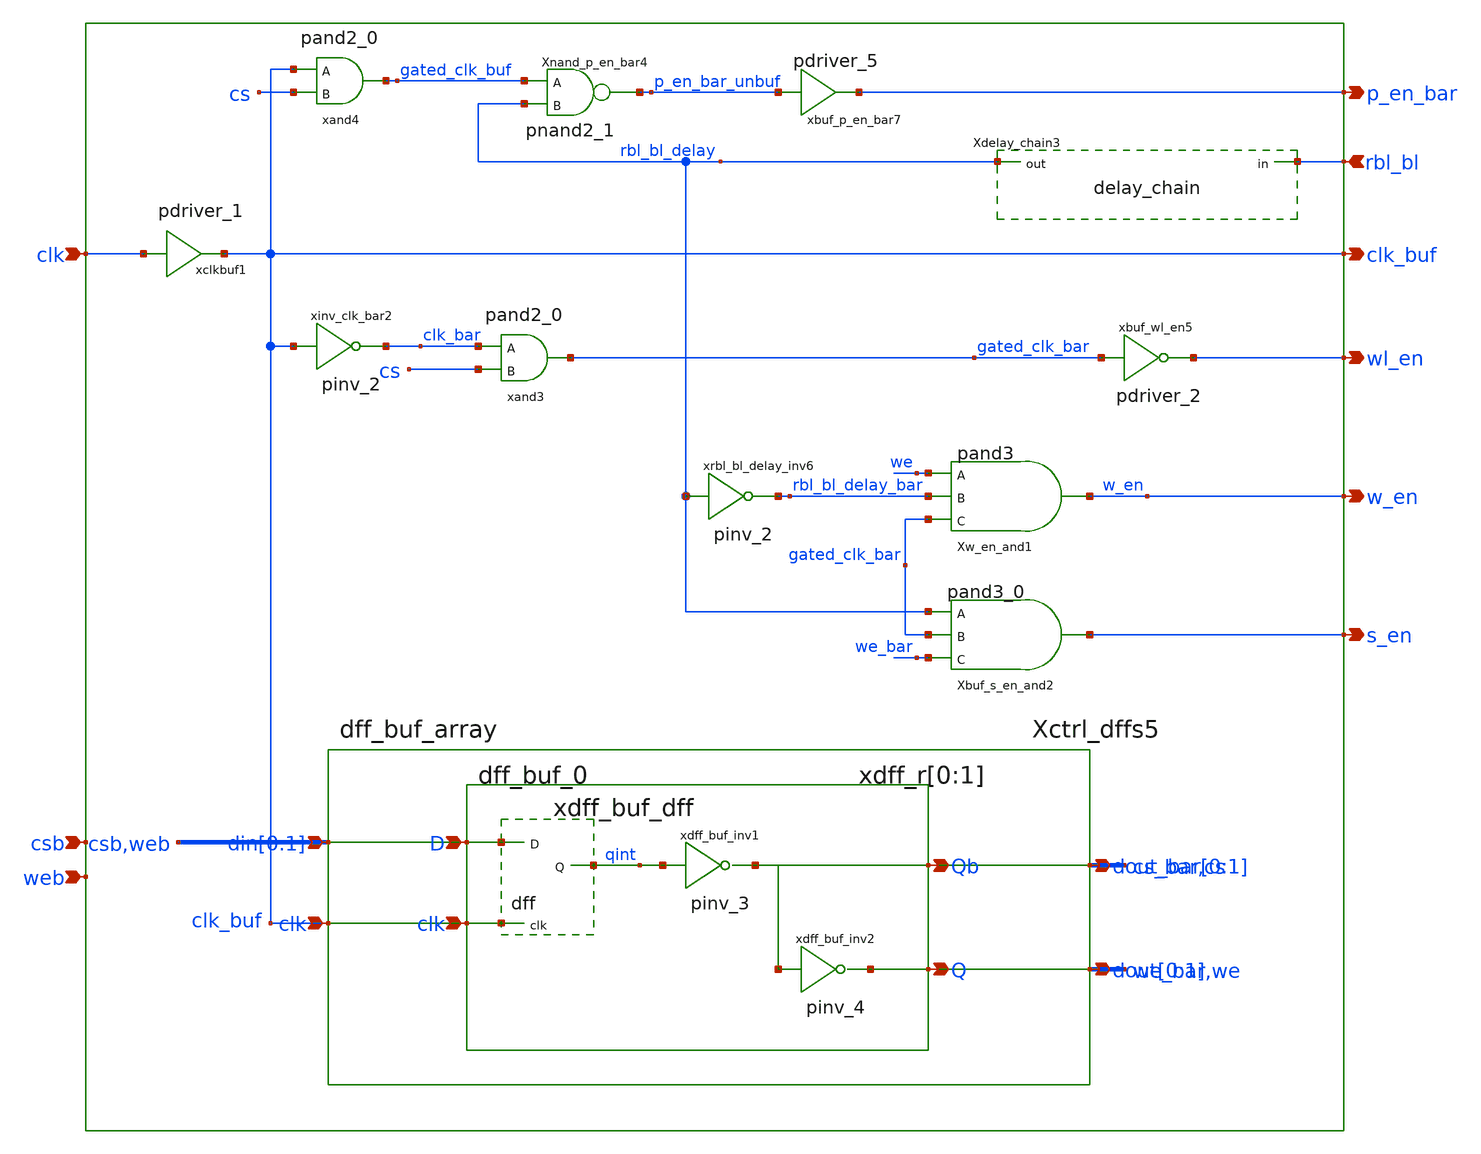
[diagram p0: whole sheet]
** sch_path: sram_2_64_scn4m_lcc/control_logic_rw.sch
**.subckt control_logic_rw clk rbl_bl s_en w_en p_en_bar wl_en csb web clk_buf
*.ipin clk
*.ipin rbl_bl
*.opin s_en
*.opin w_en
*.opin p_en_bar
*.opin wl_en
*.ipin csb
*.ipin web
*.opin clk_buf
xclkbuf1 clk clk_buf vdd gnd pdriver_1
xinv_clk_bar2 clk_buf clk_bar vdd gnd pinv_2
xand3 clk_bar cs gated_clk_bar vdd gnd pand2_0
xand4 clk_buf cs gated_clk_buf vdd gnd pand2_0
xbuf_wl_en5 gated_clk_bar wl_en vdd gnd pdriver_2
xrbl_bl_delay_inv6 rbl_bl_delay rbl_bl_delay_bar vdd gnd pinv_2
Xw_en_and1 we rbl_bl_delay_bar gated_clk_bar w_en vdd gnd pand3
Xbuf_s_en_and2 rbl_bl_delay gated_clk_bar we_bar s_en vdd gnd pand3_0
Xdelay_chain3 rbl_bl rbl_bl_delay vdd gnd delay_chain
Xnand_p_en_bar4 gated_clk_buf rbl_bl_delay p_en_bar_unbuf vdd gnd pnand2_1
xbuf_p_en_bar7 p_en_bar_unbuf p_en_bar pdriver_5
Xctrl_dffs5 csb web we_bar we cs_bar cs clk_buf vdd gnd dff_buf_array
**.ends
.end
